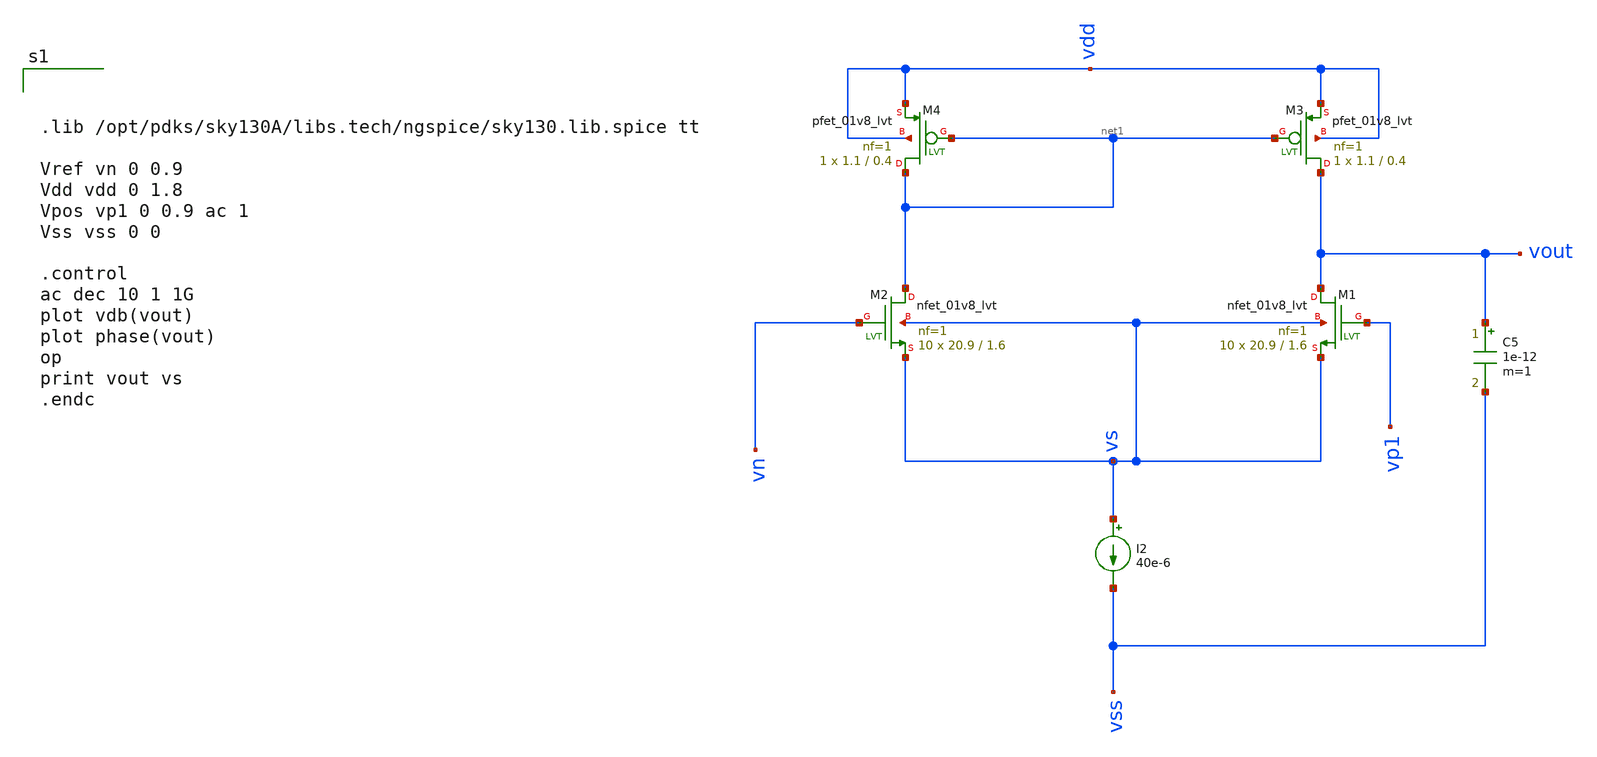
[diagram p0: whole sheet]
** sch_path: test/sstadex/xschem/ota_tb.sch
**.subckt ota_tb
I2 vs vss 40e-6
XM1 vout vp1 vs vs sky130_fd_pr__nfet_01v8_lvt L=1.6 W=20.9 nf=1 ad='int((nf+1)/2) * W/nf * 0.29' as='int((nf+2)/2) * W/nf * 0.29'
+ pd='2*int((nf+1)/2) * (W/nf + 0.29)' ps='2*int((nf+2)/2) * (W/nf + 0.29)' nrd='0.29 / W' nrs='0.29 / W'
+ sa=0 sb=0 sd=0 mult=10 m=10
XM2 net1 vn vs vs sky130_fd_pr__nfet_01v8_lvt L=1.6 W=20.9 nf=1 ad='int((nf+1)/2) * W/nf * 0.29' as='int((nf+2)/2) * W/nf * 0.29'
+ pd='2*int((nf+1)/2) * (W/nf + 0.29)' ps='2*int((nf+2)/2) * (W/nf + 0.29)' nrd='0.29 / W' nrs='0.29 / W'
+ sa=0 sb=0 sd=0 mult=10 m=10
XM3 vout net1 vdd vdd sky130_fd_pr__pfet_01v8_lvt L=0.4 W=1.1 nf=1 ad='int((nf+1)/2) * W/nf * 0.29' as='int((nf+2)/2) * W/nf * 0.29'
+ pd='2*int((nf+1)/2) * (W/nf + 0.29)' ps='2*int((nf+2)/2) * (W/nf + 0.29)' nrd='0.29 / W' nrs='0.29 / W'
+ sa=0 sb=0 sd=0 mult=1 m=1
XM4 net1 net1 vdd vdd sky130_fd_pr__pfet_01v8_lvt L=0.4 W=1.1 nf=1 ad='int((nf+1)/2) * W/nf * 0.29' as='int((nf+2)/2) * W/nf * 0.29'
+ pd='2*int((nf+1)/2) * (W/nf + 0.29)' ps='2*int((nf+2)/2) * (W/nf + 0.29)' nrd='0.29 / W' nrs='0.29 / W'
+ sa=0 sb=0 sd=0 mult=1 m=1
C5 vout vss 1e-12 m=1
**** begin user architecture code



.lib /opt/pdks/sky130A/libs.tech/ngspice/sky130.lib.spice tt

Vref vn 0 0.9
Vdd vdd 0 1.8
Vpos vp1 0 0.9 ac 1
Vss vss 0 0

.control
ac dec 10 1 1G
plot vdb(vout)
plot phase(vout)
op
print vout vs
.endc



**** end user architecture code
**.ends
.end
